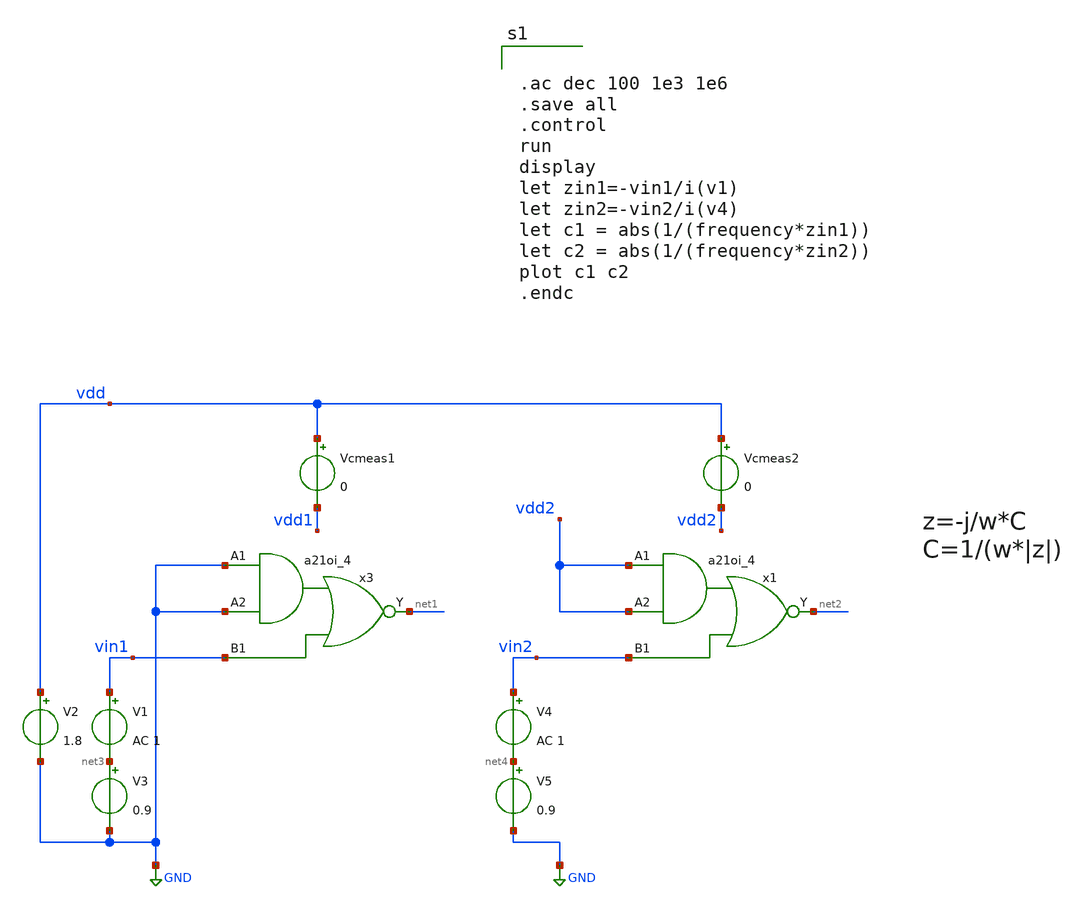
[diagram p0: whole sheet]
** sch_path: xschem/dtc_test.sch
**.subckt dtc_test
V1 vin1 net3 AC 1
V2 vdd GND 1.8
V3 net3 GND 0.9
V4 vin2 net4 AC 1
V5 net4 GND 0.9
x3 GND GND vin1 gnd gnd vdd1 vdd1 net1 sky130_fd_sc_hd__a21oi_4
x1 vdd2 vdd2 vin2 gnd gnd vdd2 vdd2 net2 sky130_fd_sc_hd__a21oi_4
Vcmeas1 vdd vdd1 0
Vcmeas2 vdd vdd2 0
**** begin user architecture code
.lib $::SKYWATER_MODELS/sky130.lib.spice tt
.include $::PDKPATH/libs.ref/sky130_fd_sc_hd/spice/sky130_fd_sc_hd.spice


.ac dec 100 1e3 1e6
.save all
.control
run
display
let zin1=-vin1/i(v1)
let zin2=-vin2/i(v4)
let c1 = abs(1/(frequency*zin1))
let c2 = abs(1/(frequency*zin2))
plot c1 c2
.endc


**** end user architecture code
**.ends
.GLOBAL GND
.end
